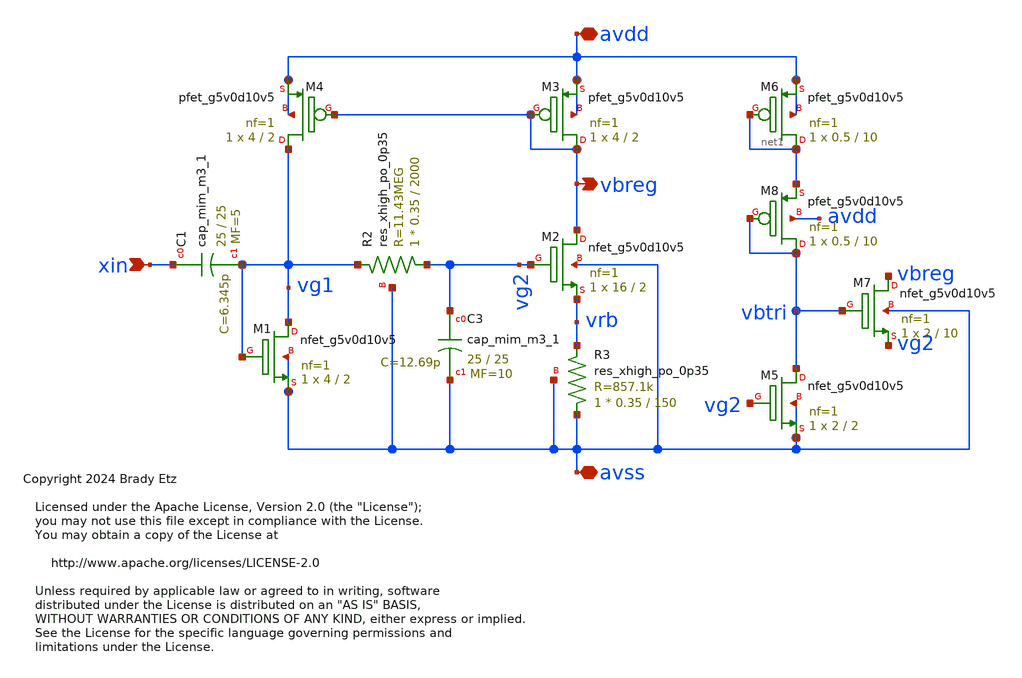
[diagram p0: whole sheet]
** sch_path: xschem/lsxo_bias_gen.sch
* Copyright 2024 Brady Etz
* Licensed under the Apache License, Version 2.0 (the "License");
**.subckt lsxo_bias_gen xin avdd avss vbreg
*.ipin xin
*.iopin avdd
*.iopin avss
*.opin vbreg
XM2 vbreg vg2 vrb avss sky130_fd_pr__nfet_g5v0d10v5 L=2 W=16 nf=1 ad='int((nf+1)/2) * W/nf * 0.29' as='int((nf+2)/2) * W/nf * 0.29'
+ pd='2*int((nf+1)/2) * (W/nf + 0.29)' ps='2*int((nf+2)/2) * (W/nf + 0.29)' nrd='0.29 / W' nrs='0.29 / W'
+ sa=0 sb=0 sd=0 mult=1 m=1
XM3 vbreg vbreg avdd avdd sky130_fd_pr__pfet_g5v0d10v5 L=2 W=4 nf=1 ad='int((nf+1)/2) * W/nf * 0.29'
+ as='int((nf+2)/2) * W/nf * 0.29' pd='2*int((nf+1)/2) * (W/nf + 0.29)' ps='2*int((nf+2)/2) * (W/nf + 0.29)'
+ nrd='0.29 / W' nrs='0.29 / W' sa=0 sb=0 sd=0 mult=1 m=1
XM4 vg1 vbreg avdd avdd sky130_fd_pr__pfet_g5v0d10v5 L=2 W=4 nf=1 ad='int((nf+1)/2) * W/nf * 0.29' as='int((nf+2)/2) * W/nf * 0.29'
+ pd='2*int((nf+1)/2) * (W/nf + 0.29)' ps='2*int((nf+2)/2) * (W/nf + 0.29)' nrd='0.29 / W' nrs='0.29 / W'
+ sa=0 sb=0 sd=0 mult=1 m=1
XM1 vg1 vg1 avss avss sky130_fd_pr__nfet_g5v0d10v5 L=2 W=4 nf=1 ad='int((nf+1)/2) * W/nf * 0.29' as='int((nf+2)/2) * W/nf * 0.29'
+ pd='2*int((nf+1)/2) * (W/nf + 0.29)' ps='2*int((nf+2)/2) * (W/nf + 0.29)' nrd='0.29 / W' nrs='0.29 / W'
+ sa=0 sb=0 sd=0 mult=1 m=1
XM6 net1 net1 avdd avdd sky130_fd_pr__pfet_g5v0d10v5 L=10 W=0.5 nf=1 ad='int((nf+1)/2) * W/nf * 0.29'
+ as='int((nf+2)/2) * W/nf * 0.29' pd='2*int((nf+1)/2) * (W/nf + 0.29)' ps='2*int((nf+2)/2) * (W/nf + 0.29)'
+ nrd='0.29 / W' nrs='0.29 / W' sa=0 sb=0 sd=0 mult=1 m=1
XM5 vbtri vg2 avss avss sky130_fd_pr__nfet_g5v0d10v5 L=2 W=2 nf=1 ad='int((nf+1)/2) * W/nf * 0.29' as='int((nf+2)/2) * W/nf * 0.29'
+ pd='2*int((nf+1)/2) * (W/nf + 0.29)' ps='2*int((nf+2)/2) * (W/nf + 0.29)' nrd='0.29 / W' nrs='0.29 / W'
+ sa=0 sb=0 sd=0 mult=1 m=1
XM7 vbreg vbtri vg2 avss sky130_fd_pr__nfet_g5v0d10v5 L=10 W=2 nf=1 ad='int((nf+1)/2) * W/nf * 0.29'
+ as='int((nf+2)/2) * W/nf * 0.29' pd='2*int((nf+1)/2) * (W/nf + 0.29)' ps='2*int((nf+2)/2) * (W/nf + 0.29)'
+ nrd='0.29 / W' nrs='0.29 / W' sa=0 sb=0 sd=0 mult=1 m=1
XM8 vbtri vbtri net1 avdd sky130_fd_pr__pfet_g5v0d10v5 L=10 W=0.5 nf=1 ad='int((nf+1)/2) * W/nf * 0.29'
+ as='int((nf+2)/2) * W/nf * 0.29' pd='2*int((nf+1)/2) * (W/nf + 0.29)' ps='2*int((nf+2)/2) * (W/nf + 0.29)'
+ nrd='0.29 / W' nrs='0.29 / W' sa=0 sb=0 sd=0 mult=1 m=1
XR2 vg2 vg1 avss sky130_fd_pr__res_xhigh_po_0p35 L=2000 mult=1 m=1
XR3 avss vrb avss sky130_fd_pr__res_xhigh_po_0p35 L=150 mult=1 m=1
XC3 vg2 avss sky130_fd_pr__cap_mim_m3_1 W=25 L=25 MF=10 m=10
XC1 xin vg1 sky130_fd_pr__cap_mim_m3_1 W=25 L=25 MF=5 m=5
**.ends
.end
